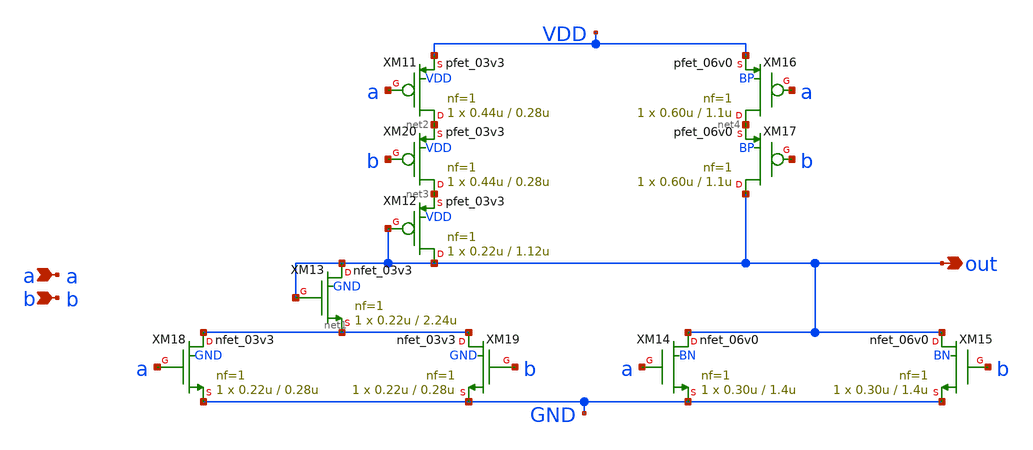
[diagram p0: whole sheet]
** sch_path: xschem_designs/NMAX.sch
**.subckt NMAX a b out
*.ipin a
*.ipin b
*.opin out
XM13 out out net1 GND nfet_03v3 L=2.24u W=0.22u nf=1 ad='int((nf+1)/2) * W/nf * 0.18u' as='int((nf+2)/2) * W/nf * 0.18u'
+ pd='2*int((nf+1)/2) * (W/nf + 0.18u)' ps='2*int((nf+2)/2) * (W/nf + 0.18u)' nrd='0.18u / W' nrs='0.18u / W'
+ sa=0 sb=0 sd=0 m=1 par=1
XM14 out a GND BN nfet_06v0 L=1.4u W=0.30u nf=1 ad='int((nf+1)/2) * W/nf * 0.18u' as='int((nf+2)/2) * W/nf * 0.18u'
+ pd='2*int((nf+1)/2) * (W/nf + 0.18u)' ps='2*int((nf+2)/2) * (W/nf + 0.18u)' nrd='0.18u / W' nrs='0.18u / W'
+ sa=0 sb=0 sd=0 m=1 par=1
XM15 out b GND BN nfet_06v0 L=1.4u W=0.30u nf=1 ad='int((nf+1)/2) * W/nf * 0.18u' as='int((nf+2)/2) * W/nf * 0.18u'
+ pd='2*int((nf+1)/2) * (W/nf + 0.18u)' ps='2*int((nf+2)/2) * (W/nf + 0.18u)' nrd='0.18u / W' nrs='0.18u / W'
+ sa=0 sb=0 sd=0 m=1 par=1
XM18 net1 a GND GND nfet_03v3 L=0.28u W=0.22u nf=1 ad='int((nf+1)/2) * W/nf * 0.18u' as='int((nf+2)/2) * W/nf * 0.18u'
+ pd='2*int((nf+1)/2) * (W/nf + 0.18u)' ps='2*int((nf+2)/2) * (W/nf + 0.18u)' nrd='0.18u / W' nrs='0.18u / W'
+ sa=0 sb=0 sd=0 m=1 par=1
XM19 net1 b GND GND nfet_03v3 L=0.28u W=0.22u nf=1 ad='int((nf+1)/2) * W/nf * 0.18u' as='int((nf+2)/2) * W/nf * 0.18u'
+ pd='2*int((nf+1)/2) * (W/nf + 0.18u)' ps='2*int((nf+2)/2) * (W/nf + 0.18u)' nrd='0.18u / W' nrs='0.18u / W'
+ sa=0 sb=0 sd=0 m=1 par=1
XM11 net2 a VDD VDD pfet_03v3 L=0.28u W=0.44u nf=1 ad='int((nf+1)/2) * W/nf * 0.18u' as='int((nf+2)/2) * W/nf * 0.18u'
+ pd='2*int((nf+1)/2) * (W/nf + 0.18u)' ps='2*int((nf+2)/2) * (W/nf + 0.18u)' nrd='0.18u / W' nrs='0.18u / W'
+ sa=0 sb=0 sd=0 m=1 par=1
XM12 out out net3 VDD pfet_03v3 L=1.12u W=0.22u nf=1 ad='int((nf+1)/2) * W/nf * 0.18u' as='int((nf+2)/2) * W/nf * 0.18u'
+ pd='2*int((nf+1)/2) * (W/nf + 0.18u)' ps='2*int((nf+2)/2) * (W/nf + 0.18u)' nrd='0.18u / W' nrs='0.18u / W'
+ sa=0 sb=0 sd=0 m=1 par=1
XM16 net4 a VDD BP pfet_06v0 L=1.1u W=0.60u nf=1 ad='int((nf+1)/2) * W/nf * 0.18u' as='int((nf+2)/2) * W/nf * 0.18u'
+ pd='2*int((nf+1)/2) * (W/nf + 0.18u)' ps='2*int((nf+2)/2) * (W/nf + 0.18u)' nrd='0.18u / W' nrs='0.18u / W'
+ sa=0 sb=0 sd=0 m=1 par=1
XM17 out b net4 BP pfet_06v0 L=1.1u W=0.60u nf=1 ad='int((nf+1)/2) * W/nf * 0.18u' as='int((nf+2)/2) * W/nf * 0.18u'
+ pd='2*int((nf+1)/2) * (W/nf + 0.18u)' ps='2*int((nf+2)/2) * (W/nf + 0.18u)' nrd='0.18u / W' nrs='0.18u / W'
+ sa=0 sb=0 sd=0 m=1 par=1
XM20 net3 b net2 VDD pfet_03v3 L=0.28u W=0.44u nf=1 ad='int((nf+1)/2) * W/nf * 0.18u' as='int((nf+2)/2) * W/nf * 0.18u'
+ pd='2*int((nf+1)/2) * (W/nf + 0.18u)' ps='2*int((nf+2)/2) * (W/nf + 0.18u)' nrd='0.18u / W' nrs='0.18u / W'
+ sa=0 sb=0 sd=0 m=1 par=1
**.ends
.end
